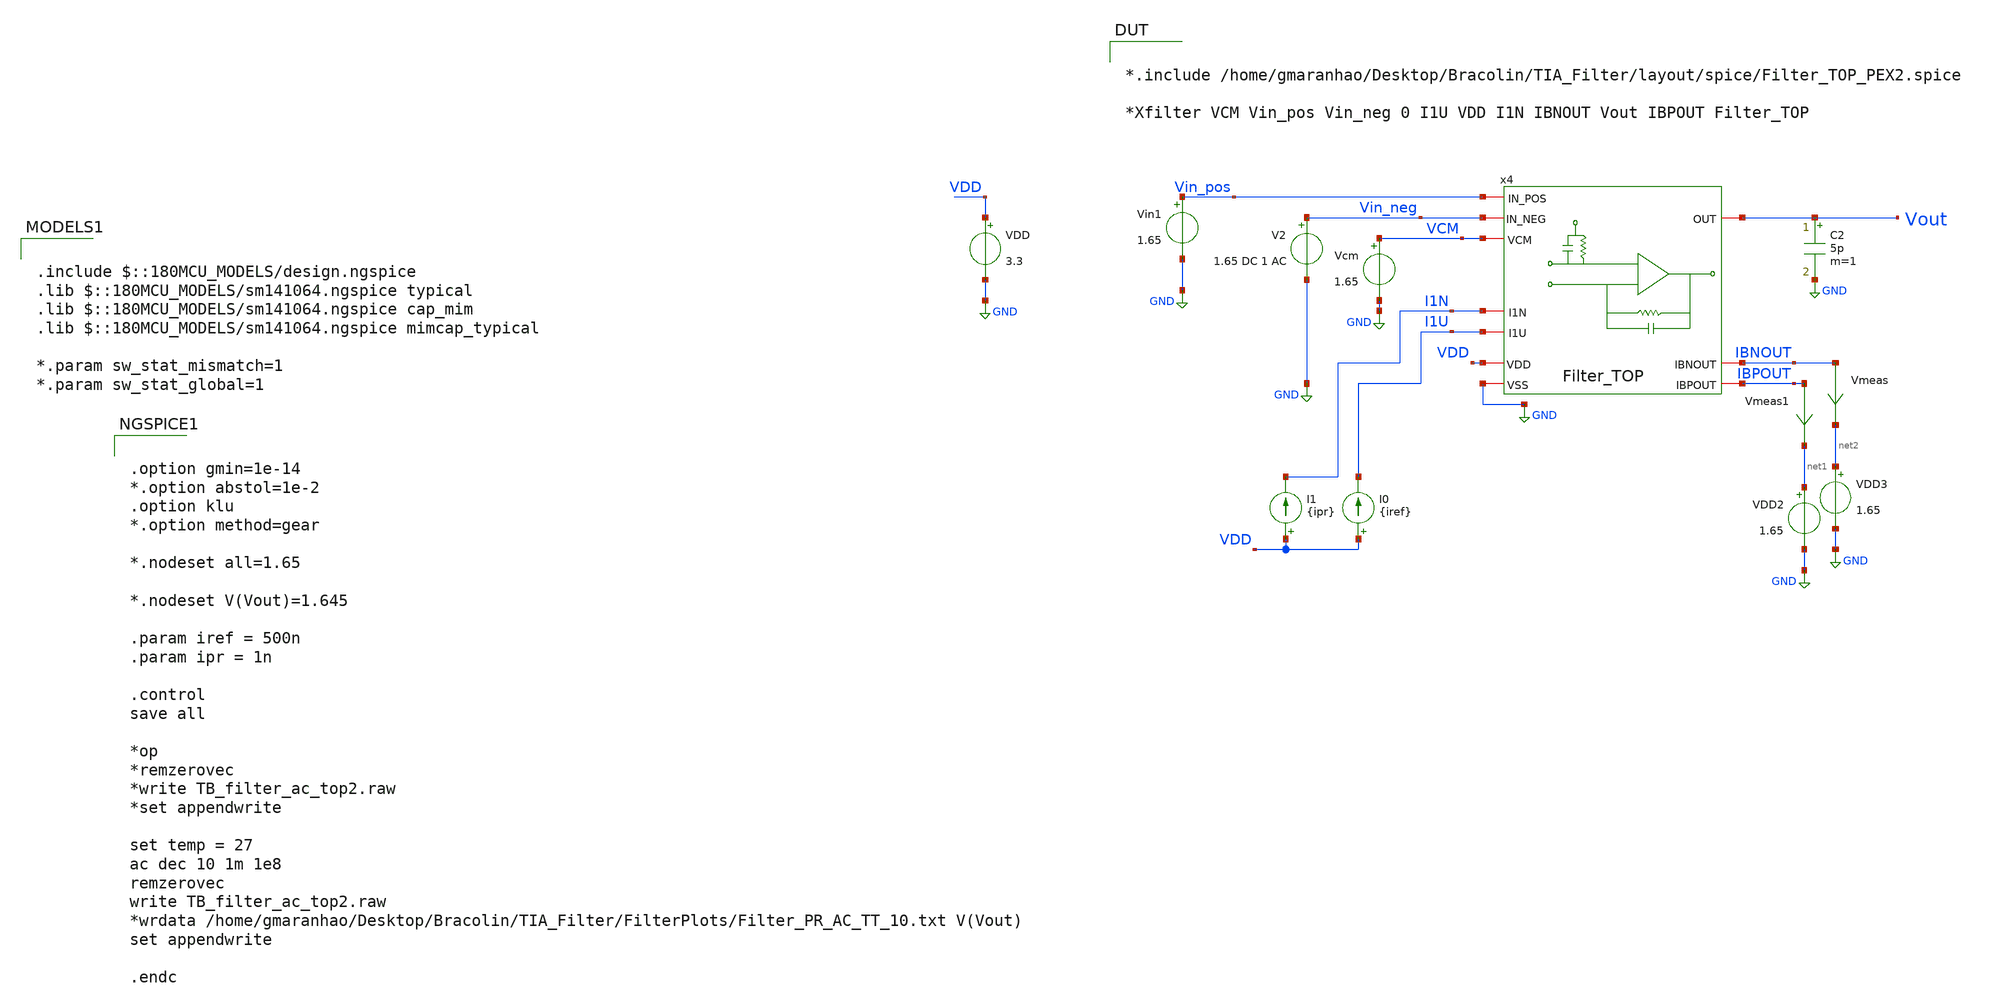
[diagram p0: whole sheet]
** sch_path: TIA_Filter/TB_filter_ac_top2.sch
**.subckt TB_filter_ac_top2
VDD VDD GND 3.3
C2 Vout GND 5p m=1
Vin1 Vin_pos GND 1.65
V2 Vin_neg GND 1.65 DC 1 AC
I0 VDD I1U {iref}
I1 VDD I1N {ipr}
Vmeas IBNOUT net2 0
.save i(vmeas)
Vmeas1 IBPOUT net1 0
.save i(vmeas1)
Vcm VCM GND 1.65
VDD2 net1 GND 1.65
VDD3 net2 GND 1.65
x4 Vin_pos Vin_neg VCM Vout VDD GND I1N I1U IBNOUT IBPOUT Filter_TOP
**** begin user architecture code

.include $::180MCU_MODELS/design.ngspice
.lib $::180MCU_MODELS/sm141064.ngspice typical
.lib $::180MCU_MODELS/sm141064.ngspice cap_mim
.lib $::180MCU_MODELS/sm141064.ngspice mimcap_typical

*.param sw_stat_mismatch=1
*.param sw_stat_global=1



.option gmin=1e-14
*.option abstol=1e-2
.option klu
*.option method=gear

*.nodeset all=1.65

*.nodeset V(Vout)=1.645

.param iref = 500n
.param ipr = 1n

.control
save all

*op
*remzerovec
*write TB_filter_ac_top2.raw
*set appendwrite

set temp = 27
ac dec 10 1m 1e8
remzerovec
write TB_filter_ac_top2.raw
*wrdata /home/gmaranhao/Desktop/Bracolin/TIA_Filter/FilterPlots/Filter_PR_AC_TT_10.txt V(Vout)
set appendwrite

.endc



*.include /home/gmaranhao/Desktop/Bracolin/TIA_Filter/layout/spice/Filter_TOP_PEX2.spice

*Xfilter VCM Vin_pos Vin_neg 0 I1U VDD I1N IBNOUT Vout IBPOUT Filter_TOP

**** end user architecture code
**.ends
.GLOBAL GND
.end
